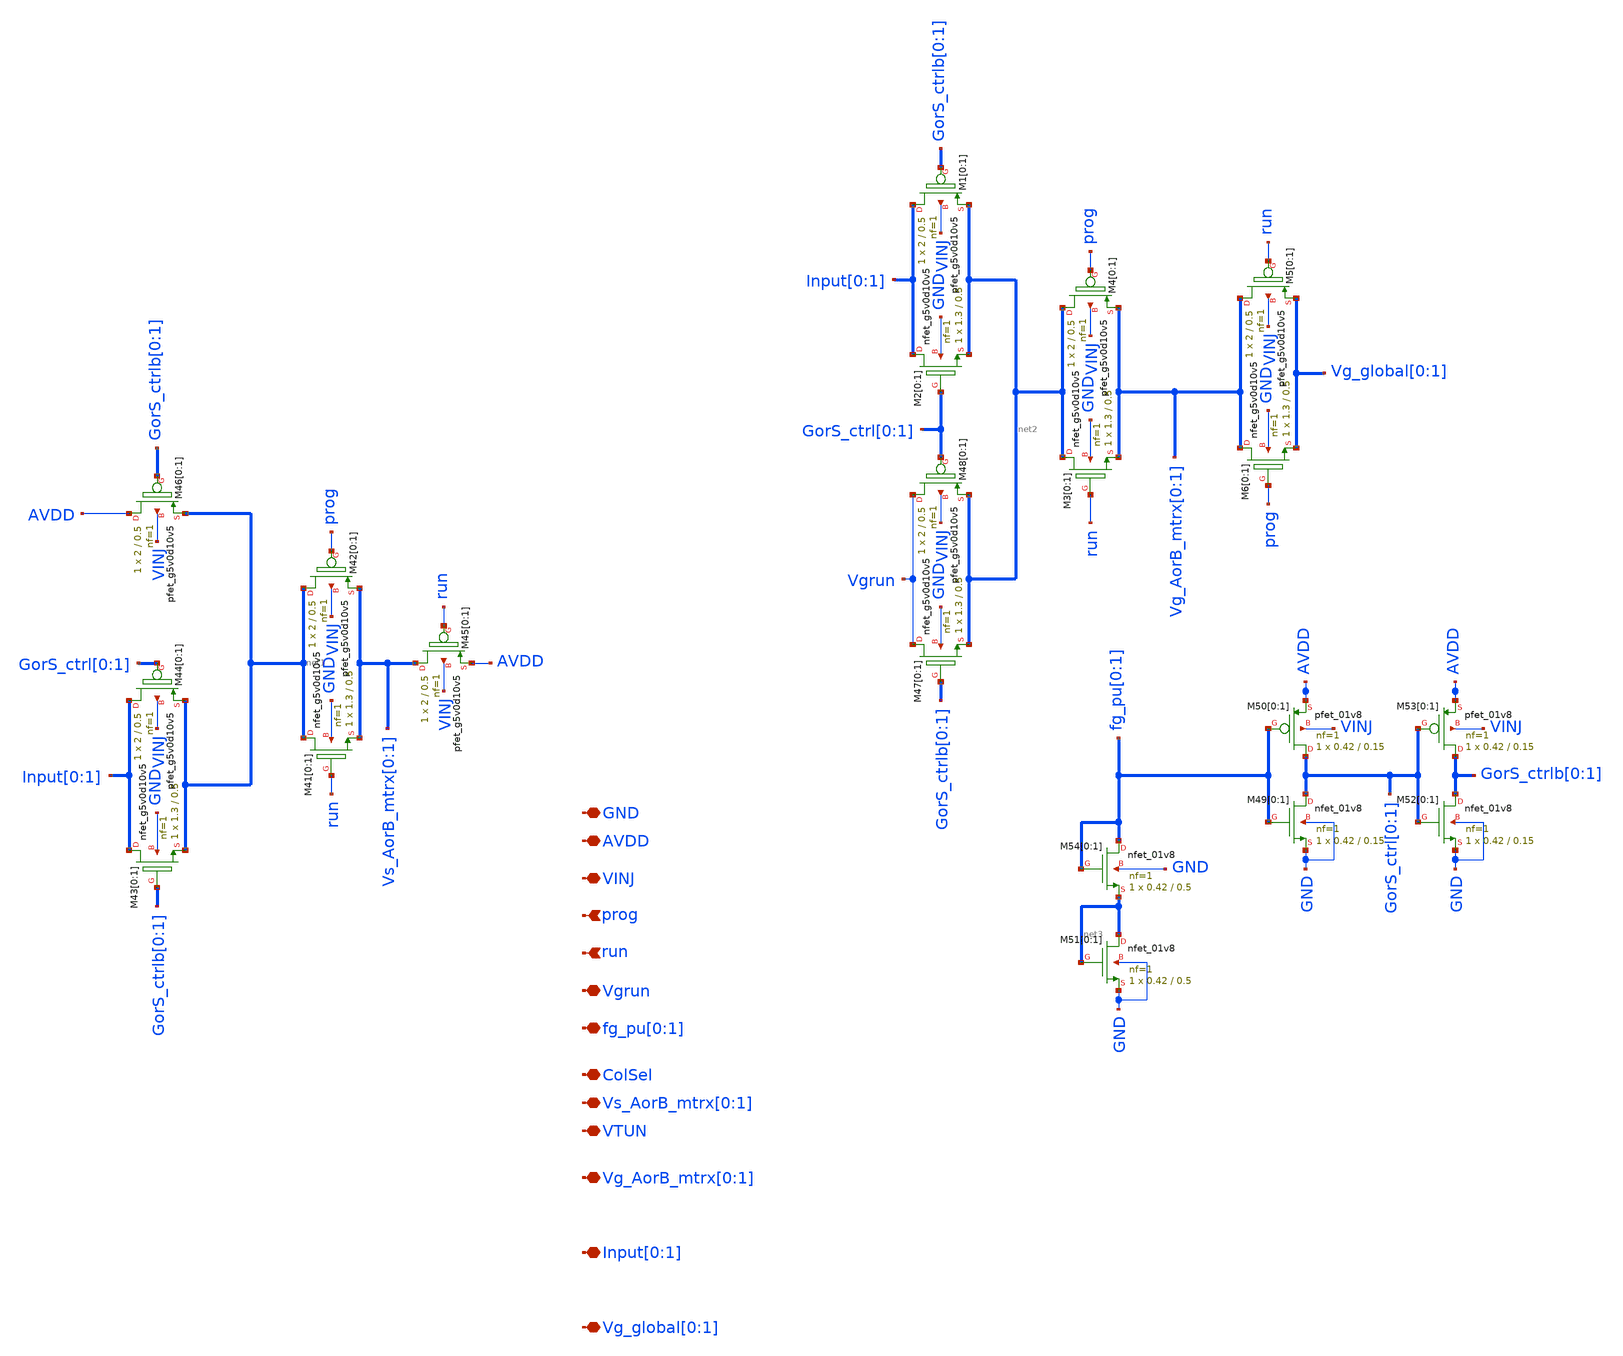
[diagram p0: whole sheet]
** sch_path: sky130_cells/G_or_S_IndrctSwcs/G_or_S_IndrctSwcsSchem.sch
**.subckt G_or_S_IndrctSwcsSchem GND AVDD VINJ Vgrun fg_pu[0],fg_pu[1]
*+ Vs_AorB_mtrx[0],Vs_AorB_mtrx[1] Vg_AorB_mtrx[0],Vg_AorB_mtrx[1] Input[0],Input[1] Vg_global[0],Vg_global[1] prog run VTUN ColSel
*.iopin GND
*.iopin AVDD
*.iopin VINJ
*.iopin Vgrun
*.iopin fg_pu[0],fg_pu[1]
*.iopin Vs_AorB_mtrx[0],Vs_AorB_mtrx[1]
*.iopin Vg_AorB_mtrx[0],Vg_AorB_mtrx[1]
*.iopin Input[0],Input[1]
*.iopin Vg_global[0],Vg_global[1]
*.ipin prog
*.ipin run
*.iopin VTUN
*.iopin ColSel
XM41[0] net1[1] run Vs_AorB_mtrx[0] GND sky130_fd_pr__nfet_g5v0d10v5 L=0.5 W=1.3 nf=1 ad='int((1 + 1)/2) * 1.3 / 1 * 0.29'
+ as='int((1 + 2)/2) * 1.3 / 1 * 0.29' pd='2*int((1 + 1)/2) * (1.3 / 1 + 0.29)' ps='2*int((1 + 2)/2) * (1.3 / 1 + 0.29)'
+ nrd='0.29 / 1.3 ' nrs='0.29 / 1.3 ' sa=0 sb=0 sd=0 mult=1 m=1
XM41[1] net1[0] run Vs_AorB_mtrx[1] GND sky130_fd_pr__nfet_g5v0d10v5 L=0.5 W=1.3 nf=1 ad='int((1 + 1)/2) * 1.3 / 1 * 0.29'
+ as='int((1 + 2)/2) * 1.3 / 1 * 0.29' pd='2*int((1 + 1)/2) * (1.3 / 1 + 0.29)' ps='2*int((1 + 2)/2) * (1.3 / 1 + 0.29)'
+ nrd='0.29 / 1.3 ' nrs='0.29 / 1.3 ' sa=0 sb=0 sd=0 mult=1 m=1
XM42[0] net1[1] prog Vs_AorB_mtrx[0] VINJ sky130_fd_pr__pfet_g5v0d10v5 L=0.5 W=2 nf=1 ad='int((1 + 1)/2) * 2 / 1 * 0.29'
+ as='int((1 + 2)/2) * 2 / 1 * 0.29' pd='2*int((1 + 1)/2) * (2 / 1 + 0.29)' ps='2*int((1 + 2)/2) * (2 / 1 + 0.29)'
+ nrd='0.29 / 2 ' nrs='0.29 / 2 ' sa=0 sb=0 sd=0 mult=1 m=1
XM42[1] net1[0] prog Vs_AorB_mtrx[1] VINJ sky130_fd_pr__pfet_g5v0d10v5 L=0.5 W=2 nf=1 ad='int((1 + 1)/2) * 2 / 1 * 0.29'
+ as='int((1 + 2)/2) * 2 / 1 * 0.29' pd='2*int((1 + 1)/2) * (2 / 1 + 0.29)' ps='2*int((1 + 2)/2) * (2 / 1 + 0.29)'
+ nrd='0.29 / 2 ' nrs='0.29 / 2 ' sa=0 sb=0 sd=0 mult=1 m=1
XM43[0] Input[0] GorS_ctrlb[0] net1[1] GND sky130_fd_pr__nfet_g5v0d10v5 L=0.5 W=1.3 nf=1 ad='int((1 + 1)/2) * 1.3 / 1 * 0.29'
+ as='int((1 + 2)/2) * 1.3 / 1 * 0.29' pd='2*int((1 + 1)/2) * (1.3 / 1 + 0.29)' ps='2*int((1 + 2)/2) * (1.3 / 1 + 0.29)'
+ nrd='0.29 / 1.3 ' nrs='0.29 / 1.3 ' sa=0 sb=0 sd=0 mult=1 m=1
XM43[1] Input[1] GorS_ctrlb[1] net1[0] GND sky130_fd_pr__nfet_g5v0d10v5 L=0.5 W=1.3 nf=1 ad='int((1 + 1)/2) * 1.3 / 1 * 0.29'
+ as='int((1 + 2)/2) * 1.3 / 1 * 0.29' pd='2*int((1 + 1)/2) * (1.3 / 1 + 0.29)' ps='2*int((1 + 2)/2) * (1.3 / 1 + 0.29)'
+ nrd='0.29 / 1.3 ' nrs='0.29 / 1.3 ' sa=0 sb=0 sd=0 mult=1 m=1
XM44[0] Input[0] GorS_ctrl[0] net1[1] VINJ sky130_fd_pr__pfet_g5v0d10v5 L=0.5 W=2 nf=1 ad='int((1 + 1)/2) * 2 / 1 * 0.29'
+ as='int((1 + 2)/2) * 2 / 1 * 0.29' pd='2*int((1 + 1)/2) * (2 / 1 + 0.29)' ps='2*int((1 + 2)/2) * (2 / 1 + 0.29)'
+ nrd='0.29 / 2 ' nrs='0.29 / 2 ' sa=0 sb=0 sd=0 mult=1 m=1
XM44[1] Input[1] GorS_ctrl[1] net1[0] VINJ sky130_fd_pr__pfet_g5v0d10v5 L=0.5 W=2 nf=1 ad='int((1 + 1)/2) * 2 / 1 * 0.29'
+ as='int((1 + 2)/2) * 2 / 1 * 0.29' pd='2*int((1 + 1)/2) * (2 / 1 + 0.29)' ps='2*int((1 + 2)/2) * (2 / 1 + 0.29)'
+ nrd='0.29 / 2 ' nrs='0.29 / 2 ' sa=0 sb=0 sd=0 mult=1 m=1
XM45[0] Vs_AorB_mtrx[0] run AVDD VINJ sky130_fd_pr__pfet_g5v0d10v5 L=0.5 W=2 nf=1 ad='int((1 + 1)/2) * 2 / 1 * 0.29'
+ as='int((1 + 2)/2) * 2 / 1 * 0.29' pd='2*int((1 + 1)/2) * (2 / 1 + 0.29)' ps='2*int((1 + 2)/2) * (2 / 1 + 0.29)'
+ nrd='0.29 / 2 ' nrs='0.29 / 2 ' sa=0 sb=0 sd=0 mult=1 m=1
XM45[1] Vs_AorB_mtrx[1] run AVDD VINJ sky130_fd_pr__pfet_g5v0d10v5 L=0.5 W=2 nf=1 ad='int((1 + 1)/2) * 2 / 1 * 0.29'
+ as='int((1 + 2)/2) * 2 / 1 * 0.29' pd='2*int((1 + 1)/2) * (2 / 1 + 0.29)' ps='2*int((1 + 2)/2) * (2 / 1 + 0.29)'
+ nrd='0.29 / 2 ' nrs='0.29 / 2 ' sa=0 sb=0 sd=0 mult=1 m=1
XM46[0] AVDD GorS_ctrlb[0] net1[1] VINJ sky130_fd_pr__pfet_g5v0d10v5 L=0.5 W=2 nf=1 ad='int((1 + 1)/2) * 2 / 1 * 0.29'
+ as='int((1 + 2)/2) * 2 / 1 * 0.29' pd='2*int((1 + 1)/2) * (2 / 1 + 0.29)' ps='2*int((1 + 2)/2) * (2 / 1 + 0.29)'
+ nrd='0.29 / 2 ' nrs='0.29 / 2 ' sa=0 sb=0 sd=0 mult=1 m=1
XM46[1] AVDD GorS_ctrlb[1] net1[0] VINJ sky130_fd_pr__pfet_g5v0d10v5 L=0.5 W=2 nf=1 ad='int((1 + 1)/2) * 2 / 1 * 0.29'
+ as='int((1 + 2)/2) * 2 / 1 * 0.29' pd='2*int((1 + 1)/2) * (2 / 1 + 0.29)' ps='2*int((1 + 2)/2) * (2 / 1 + 0.29)'
+ nrd='0.29 / 2 ' nrs='0.29 / 2 ' sa=0 sb=0 sd=0 mult=1 m=1
XM2[0] Input[0] GorS_ctrl[0] net2[1] GND sky130_fd_pr__nfet_g5v0d10v5 L=0.5 W=1.3 nf=1 ad='int((1 + 1)/2) * 1.3 / 1 * 0.29'
+ as='int((1 + 2)/2) * 1.3 / 1 * 0.29' pd='2*int((1 + 1)/2) * (1.3 / 1 + 0.29)' ps='2*int((1 + 2)/2) * (1.3 / 1 + 0.29)'
+ nrd='0.29 / 1.3 ' nrs='0.29 / 1.3 ' sa=0 sb=0 sd=0 mult=1 m=1
XM2[1] Input[1] GorS_ctrl[1] net2[0] GND sky130_fd_pr__nfet_g5v0d10v5 L=0.5 W=1.3 nf=1 ad='int((1 + 1)/2) * 1.3 / 1 * 0.29'
+ as='int((1 + 2)/2) * 1.3 / 1 * 0.29' pd='2*int((1 + 1)/2) * (1.3 / 1 + 0.29)' ps='2*int((1 + 2)/2) * (1.3 / 1 + 0.29)'
+ nrd='0.29 / 1.3 ' nrs='0.29 / 1.3 ' sa=0 sb=0 sd=0 mult=1 m=1
XM1[0] Input[0] GorS_ctrlb[0] net2[1] VINJ sky130_fd_pr__pfet_g5v0d10v5 L=0.5 W=2 nf=1 ad='int((1 + 1)/2) * 2 / 1 * 0.29'
+ as='int((1 + 2)/2) * 2 / 1 * 0.29' pd='2*int((1 + 1)/2) * (2 / 1 + 0.29)' ps='2*int((1 + 2)/2) * (2 / 1 + 0.29)'
+ nrd='0.29 / 2 ' nrs='0.29 / 2 ' sa=0 sb=0 sd=0 mult=1 m=1
XM1[1] Input[1] GorS_ctrlb[1] net2[0] VINJ sky130_fd_pr__pfet_g5v0d10v5 L=0.5 W=2 nf=1 ad='int((1 + 1)/2) * 2 / 1 * 0.29'
+ as='int((1 + 2)/2) * 2 / 1 * 0.29' pd='2*int((1 + 1)/2) * (2 / 1 + 0.29)' ps='2*int((1 + 2)/2) * (2 / 1 + 0.29)'
+ nrd='0.29 / 2 ' nrs='0.29 / 2 ' sa=0 sb=0 sd=0 mult=1 m=1
XM3[0] net2[1] run Vg_AorB_mtrx[0] GND sky130_fd_pr__nfet_g5v0d10v5 L=0.5 W=1.3 nf=1 ad='int((1 + 1)/2) * 1.3 / 1 * 0.29'
+ as='int((1 + 2)/2) * 1.3 / 1 * 0.29' pd='2*int((1 + 1)/2) * (1.3 / 1 + 0.29)' ps='2*int((1 + 2)/2) * (1.3 / 1 + 0.29)'
+ nrd='0.29 / 1.3 ' nrs='0.29 / 1.3 ' sa=0 sb=0 sd=0 mult=1 m=1
XM3[1] net2[0] run Vg_AorB_mtrx[1] GND sky130_fd_pr__nfet_g5v0d10v5 L=0.5 W=1.3 nf=1 ad='int((1 + 1)/2) * 1.3 / 1 * 0.29'
+ as='int((1 + 2)/2) * 1.3 / 1 * 0.29' pd='2*int((1 + 1)/2) * (1.3 / 1 + 0.29)' ps='2*int((1 + 2)/2) * (1.3 / 1 + 0.29)'
+ nrd='0.29 / 1.3 ' nrs='0.29 / 1.3 ' sa=0 sb=0 sd=0 mult=1 m=1
XM4[0] net2[1] prog Vg_AorB_mtrx[0] VINJ sky130_fd_pr__pfet_g5v0d10v5 L=0.5 W=2 nf=1 ad='int((1 + 1)/2) * 2 / 1 * 0.29'
+ as='int((1 + 2)/2) * 2 / 1 * 0.29' pd='2*int((1 + 1)/2) * (2 / 1 + 0.29)' ps='2*int((1 + 2)/2) * (2 / 1 + 0.29)'
+ nrd='0.29 / 2 ' nrs='0.29 / 2 ' sa=0 sb=0 sd=0 mult=1 m=1
XM4[1] net2[0] prog Vg_AorB_mtrx[1] VINJ sky130_fd_pr__pfet_g5v0d10v5 L=0.5 W=2 nf=1 ad='int((1 + 1)/2) * 2 / 1 * 0.29'
+ as='int((1 + 2)/2) * 2 / 1 * 0.29' pd='2*int((1 + 1)/2) * (2 / 1 + 0.29)' ps='2*int((1 + 2)/2) * (2 / 1 + 0.29)'
+ nrd='0.29 / 2 ' nrs='0.29 / 2 ' sa=0 sb=0 sd=0 mult=1 m=1
XM6[0] Vg_AorB_mtrx[0] prog Vg_global[0] GND sky130_fd_pr__nfet_g5v0d10v5 L=0.5 W=1.3 nf=1 ad='int((1 + 1)/2) * 1.3 / 1 * 0.29'
+ as='int((1 + 2)/2) * 1.3 / 1 * 0.29' pd='2*int((1 + 1)/2) * (1.3 / 1 + 0.29)' ps='2*int((1 + 2)/2) * (1.3 / 1 + 0.29)'
+ nrd='0.29 / 1.3 ' nrs='0.29 / 1.3 ' sa=0 sb=0 sd=0 mult=1 m=1
XM6[1] Vg_AorB_mtrx[1] prog Vg_global[1] GND sky130_fd_pr__nfet_g5v0d10v5 L=0.5 W=1.3 nf=1 ad='int((1 + 1)/2) * 1.3 / 1 * 0.29'
+ as='int((1 + 2)/2) * 1.3 / 1 * 0.29' pd='2*int((1 + 1)/2) * (1.3 / 1 + 0.29)' ps='2*int((1 + 2)/2) * (1.3 / 1 + 0.29)'
+ nrd='0.29 / 1.3 ' nrs='0.29 / 1.3 ' sa=0 sb=0 sd=0 mult=1 m=1
XM5[0] Vg_AorB_mtrx[0] run Vg_global[0] VINJ sky130_fd_pr__pfet_g5v0d10v5 L=0.5 W=2 nf=1 ad='int((1 + 1)/2) * 2 / 1 * 0.29'
+ as='int((1 + 2)/2) * 2 / 1 * 0.29' pd='2*int((1 + 1)/2) * (2 / 1 + 0.29)' ps='2*int((1 + 2)/2) * (2 / 1 + 0.29)'
+ nrd='0.29 / 2 ' nrs='0.29 / 2 ' sa=0 sb=0 sd=0 mult=1 m=1
XM5[1] Vg_AorB_mtrx[1] run Vg_global[1] VINJ sky130_fd_pr__pfet_g5v0d10v5 L=0.5 W=2 nf=1 ad='int((1 + 1)/2) * 2 / 1 * 0.29'
+ as='int((1 + 2)/2) * 2 / 1 * 0.29' pd='2*int((1 + 1)/2) * (2 / 1 + 0.29)' ps='2*int((1 + 2)/2) * (2 / 1 + 0.29)'
+ nrd='0.29 / 2 ' nrs='0.29 / 2 ' sa=0 sb=0 sd=0 mult=1 m=1
XM47[0] Vgrun GorS_ctrlb[0] net2[1] GND sky130_fd_pr__nfet_g5v0d10v5 L=0.5 W=1.3 nf=1 ad='int((1 + 1)/2) * 1.3 / 1 * 0.29'
+ as='int((1 + 2)/2) * 1.3 / 1 * 0.29' pd='2*int((1 + 1)/2) * (1.3 / 1 + 0.29)' ps='2*int((1 + 2)/2) * (1.3 / 1 + 0.29)'
+ nrd='0.29 / 1.3 ' nrs='0.29 / 1.3 ' sa=0 sb=0 sd=0 mult=1 m=1
XM47[1] Vgrun GorS_ctrlb[1] net2[0] GND sky130_fd_pr__nfet_g5v0d10v5 L=0.5 W=1.3 nf=1 ad='int((1 + 1)/2) * 1.3 / 1 * 0.29'
+ as='int((1 + 2)/2) * 1.3 / 1 * 0.29' pd='2*int((1 + 1)/2) * (1.3 / 1 + 0.29)' ps='2*int((1 + 2)/2) * (1.3 / 1 + 0.29)'
+ nrd='0.29 / 1.3 ' nrs='0.29 / 1.3 ' sa=0 sb=0 sd=0 mult=1 m=1
XM48[0] Vgrun GorS_ctrl[0] net2[1] VINJ sky130_fd_pr__pfet_g5v0d10v5 L=0.5 W=2 nf=1 ad='int((1 + 1)/2) * 2 / 1 * 0.29'
+ as='int((1 + 2)/2) * 2 / 1 * 0.29' pd='2*int((1 + 1)/2) * (2 / 1 + 0.29)' ps='2*int((1 + 2)/2) * (2 / 1 + 0.29)'
+ nrd='0.29 / 2 ' nrs='0.29 / 2 ' sa=0 sb=0 sd=0 mult=1 m=1
XM48[1] Vgrun GorS_ctrl[1] net2[0] VINJ sky130_fd_pr__pfet_g5v0d10v5 L=0.5 W=2 nf=1 ad='int((1 + 1)/2) * 2 / 1 * 0.29'
+ as='int((1 + 2)/2) * 2 / 1 * 0.29' pd='2*int((1 + 1)/2) * (2 / 1 + 0.29)' ps='2*int((1 + 2)/2) * (2 / 1 + 0.29)'
+ nrd='0.29 / 2 ' nrs='0.29 / 2 ' sa=0 sb=0 sd=0 mult=1 m=1
XM49[0] GorS_ctrl[0] fg_pu[0] GND GND sky130_fd_pr__nfet_01v8 L=0.15 W=0.42 nf=1 ad='int((1 + 1)/2) * 0.42 / 1 * 0.29'
+ as='int((1 + 2)/2) * 0.42 / 1 * 0.29' pd='2*int((1 + 1)/2) * (0.42 / 1 + 0.29)' ps='2*int((1 + 2)/2) * (0.42 / 1 + 0.29)'
+ nrd='0.29 / 0.42 ' nrs='0.29 / 0.42 ' sa=0 sb=0 sd=0 mult=1 m=1
XM49[1] GorS_ctrl[1] fg_pu[1] GND GND sky130_fd_pr__nfet_01v8 L=0.15 W=0.42 nf=1 ad='int((1 + 1)/2) * 0.42 / 1 * 0.29'
+ as='int((1 + 2)/2) * 0.42 / 1 * 0.29' pd='2*int((1 + 1)/2) * (0.42 / 1 + 0.29)' ps='2*int((1 + 2)/2) * (0.42 / 1 + 0.29)'
+ nrd='0.29 / 0.42 ' nrs='0.29 / 0.42 ' sa=0 sb=0 sd=0 mult=1 m=1
XM50[0] GorS_ctrl[0] fg_pu[0] AVDD VINJ sky130_fd_pr__pfet_01v8 L=0.15 W=0.42 nf=1 ad='int((1 + 1)/2) * 0.42 / 1 * 0.29'
+ as='int((1 + 2)/2) * 0.42 / 1 * 0.29' pd='2*int((1 + 1)/2) * (0.42 / 1 + 0.29)' ps='2*int((1 + 2)/2) * (0.42 / 1 + 0.29)'
+ nrd='0.29 / 0.42 ' nrs='0.29 / 0.42 ' sa=0 sb=0 sd=0 mult=1 m=1
XM50[1] GorS_ctrl[1] fg_pu[1] AVDD VINJ sky130_fd_pr__pfet_01v8 L=0.15 W=0.42 nf=1 ad='int((1 + 1)/2) * 0.42 / 1 * 0.29'
+ as='int((1 + 2)/2) * 0.42 / 1 * 0.29' pd='2*int((1 + 1)/2) * (0.42 / 1 + 0.29)' ps='2*int((1 + 2)/2) * (0.42 / 1 + 0.29)'
+ nrd='0.29 / 0.42 ' nrs='0.29 / 0.42 ' sa=0 sb=0 sd=0 mult=1 m=1
XM51[0] net3[1] net3[1] GND GND sky130_fd_pr__nfet_01v8 L=0.5 W=0.42 nf=1 ad='int((1 + 1)/2) * 0.42 / 1 * 0.29'
+ as='int((1 + 2)/2) * 0.42 / 1 * 0.29' pd='2*int((1 + 1)/2) * (0.42 / 1 + 0.29)' ps='2*int((1 + 2)/2) * (0.42 / 1 + 0.29)'
+ nrd='0.29 / 0.42 ' nrs='0.29 / 0.42 ' sa=0 sb=0 sd=0 mult=1 m=1
XM51[1] net3[0] net3[0] GND GND sky130_fd_pr__nfet_01v8 L=0.5 W=0.42 nf=1 ad='int((1 + 1)/2) * 0.42 / 1 * 0.29'
+ as='int((1 + 2)/2) * 0.42 / 1 * 0.29' pd='2*int((1 + 1)/2) * (0.42 / 1 + 0.29)' ps='2*int((1 + 2)/2) * (0.42 / 1 + 0.29)'
+ nrd='0.29 / 0.42 ' nrs='0.29 / 0.42 ' sa=0 sb=0 sd=0 mult=1 m=1
XM52[0] GorS_ctrlb[0] GorS_ctrl[0] GND GND sky130_fd_pr__nfet_01v8 L=0.15 W=0.42 nf=1 ad='int((1 + 1)/2) * 0.42 / 1 * 0.29'
+ as='int((1 + 2)/2) * 0.42 / 1 * 0.29' pd='2*int((1 + 1)/2) * (0.42 / 1 + 0.29)' ps='2*int((1 + 2)/2) * (0.42 / 1 + 0.29)'
+ nrd='0.29 / 0.42 ' nrs='0.29 / 0.42 ' sa=0 sb=0 sd=0 mult=1 m=1
XM52[1] GorS_ctrlb[1] GorS_ctrl[1] GND GND sky130_fd_pr__nfet_01v8 L=0.15 W=0.42 nf=1 ad='int((1 + 1)/2) * 0.42 / 1 * 0.29'
+ as='int((1 + 2)/2) * 0.42 / 1 * 0.29' pd='2*int((1 + 1)/2) * (0.42 / 1 + 0.29)' ps='2*int((1 + 2)/2) * (0.42 / 1 + 0.29)'
+ nrd='0.29 / 0.42 ' nrs='0.29 / 0.42 ' sa=0 sb=0 sd=0 mult=1 m=1
XM53[0] GorS_ctrlb[0] GorS_ctrl[0] AVDD VINJ sky130_fd_pr__pfet_01v8 L=0.15 W=0.42 nf=1 ad='int((1 + 1)/2) * 0.42 / 1 * 0.29'
+ as='int((1 + 2)/2) * 0.42 / 1 * 0.29' pd='2*int((1 + 1)/2) * (0.42 / 1 + 0.29)' ps='2*int((1 + 2)/2) * (0.42 / 1 + 0.29)'
+ nrd='0.29 / 0.42 ' nrs='0.29 / 0.42 ' sa=0 sb=0 sd=0 mult=1 m=1
XM53[1] GorS_ctrlb[1] GorS_ctrl[1] AVDD VINJ sky130_fd_pr__pfet_01v8 L=0.15 W=0.42 nf=1 ad='int((1 + 1)/2) * 0.42 / 1 * 0.29'
+ as='int((1 + 2)/2) * 0.42 / 1 * 0.29' pd='2*int((1 + 1)/2) * (0.42 / 1 + 0.29)' ps='2*int((1 + 2)/2) * (0.42 / 1 + 0.29)'
+ nrd='0.29 / 0.42 ' nrs='0.29 / 0.42 ' sa=0 sb=0 sd=0 mult=1 m=1
XM54[0] fg_pu[0] fg_pu[0] net3[1] GND sky130_fd_pr__nfet_01v8 L=0.5 W=0.42 nf=1 ad='int((1 + 1)/2) * 0.42 / 1 * 0.29'
+ as='int((1 + 2)/2) * 0.42 / 1 * 0.29' pd='2*int((1 + 1)/2) * (0.42 / 1 + 0.29)' ps='2*int((1 + 2)/2) * (0.42 / 1 + 0.29)'
+ nrd='0.29 / 0.42 ' nrs='0.29 / 0.42 ' sa=0 sb=0 sd=0 mult=1 m=1
XM54[1] fg_pu[1] fg_pu[1] net3[0] GND sky130_fd_pr__nfet_01v8 L=0.5 W=0.42 nf=1 ad='int((1 + 1)/2) * 0.42 / 1 * 0.29'
+ as='int((1 + 2)/2) * 0.42 / 1 * 0.29' pd='2*int((1 + 1)/2) * (0.42 / 1 + 0.29)' ps='2*int((1 + 2)/2) * (0.42 / 1 + 0.29)'
+ nrd='0.29 / 0.42 ' nrs='0.29 / 0.42 ' sa=0 sb=0 sd=0 mult=1 m=1
**.ends
.end
